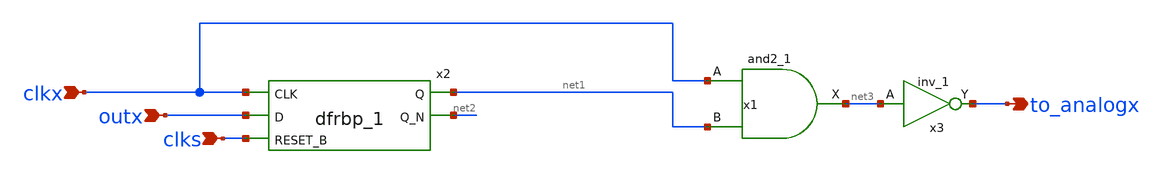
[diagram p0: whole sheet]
** sch_path: one_switch_for_symbol.sch
**.subckt one_switch_for_symbol clkx outx clks to_analogx
*.ipin clkx
*.ipin outx
*.ipin clks
*.opin to_analogx
x2 clkx outx clks VGND VNB VPB VPWR net1 net2 sky130_fd_sc_hd__dfrbp_1
x1 clkx net1 VGND VNB VPB VPWR net3 sky130_fd_sc_hd__and2_1
x3 net3 VGND VNB VPB VPWR to_analogx sky130_fd_sc_hd__inv_1
**.ends
.end
